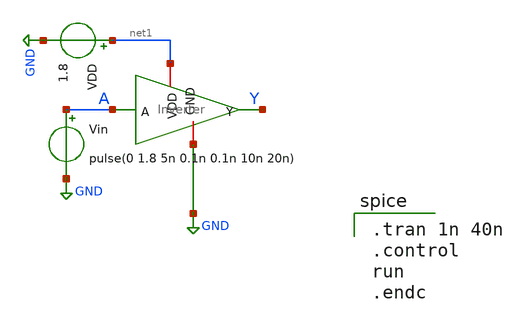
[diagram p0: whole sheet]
** sch_path: inverter/Inverter_Testbench.sch
**.subckt Inverter_Testbench
x1 net1 A Y net2 Inverter
Vin A GND pulse(0 1.8 5n 0.1n 0.1n 10n 20n)
VDD net1 GND 1.8
**** begin user architecture code
 .lib $::SKYWATER_MODELS/sky130.lib.spice tt

.tran 1n 40n
.control
run
.endc

**** end user architecture code
**.ends

* expanding   symbol:  /home/ee431/workspace/inverter/Inverter.sym # of pins=4
** sym_path: inverter/Inverter.sym
** sch_path: inverter/Inverter.sch
.subckt Inverter VDD A Y GND
*.ipin A
*.opin Y
*.iopin VDD
*.iopin GND
XM1 Y A VDD VDD sky130_fd_pr__pfet_01v8 L=0.5 W=2 nf=1 ad='int((nf+1)/2) * W/nf * 0.29' as='int((nf+2)/2) * W/nf * 0.29'
+ pd='2*int((nf+1)/2) * (W/nf + 0.29)' ps='2*int((nf+2)/2) * (W/nf + 0.29)' nrd='0.29 / W' nrs='0.29 / W'
+ sa=0 sb=0 sd=0 mult=1 m=1
XM2 Y A GND GND sky130_fd_pr__nfet_01v8 L=0.5 W=1 nf=1 ad='int((nf+1)/2) * W/nf * 0.29' as='int((nf+2)/2) * W/nf * 0.29'
+ pd='2*int((nf+1)/2) * (W/nf + 0.29)' ps='2*int((nf+2)/2) * (W/nf + 0.29)' nrd='0.29 / W' nrs='0.29 / W'
+ sa=0 sb=0 sd=0 mult=1 m=1
.ends

.GLOBAL GND
.end
